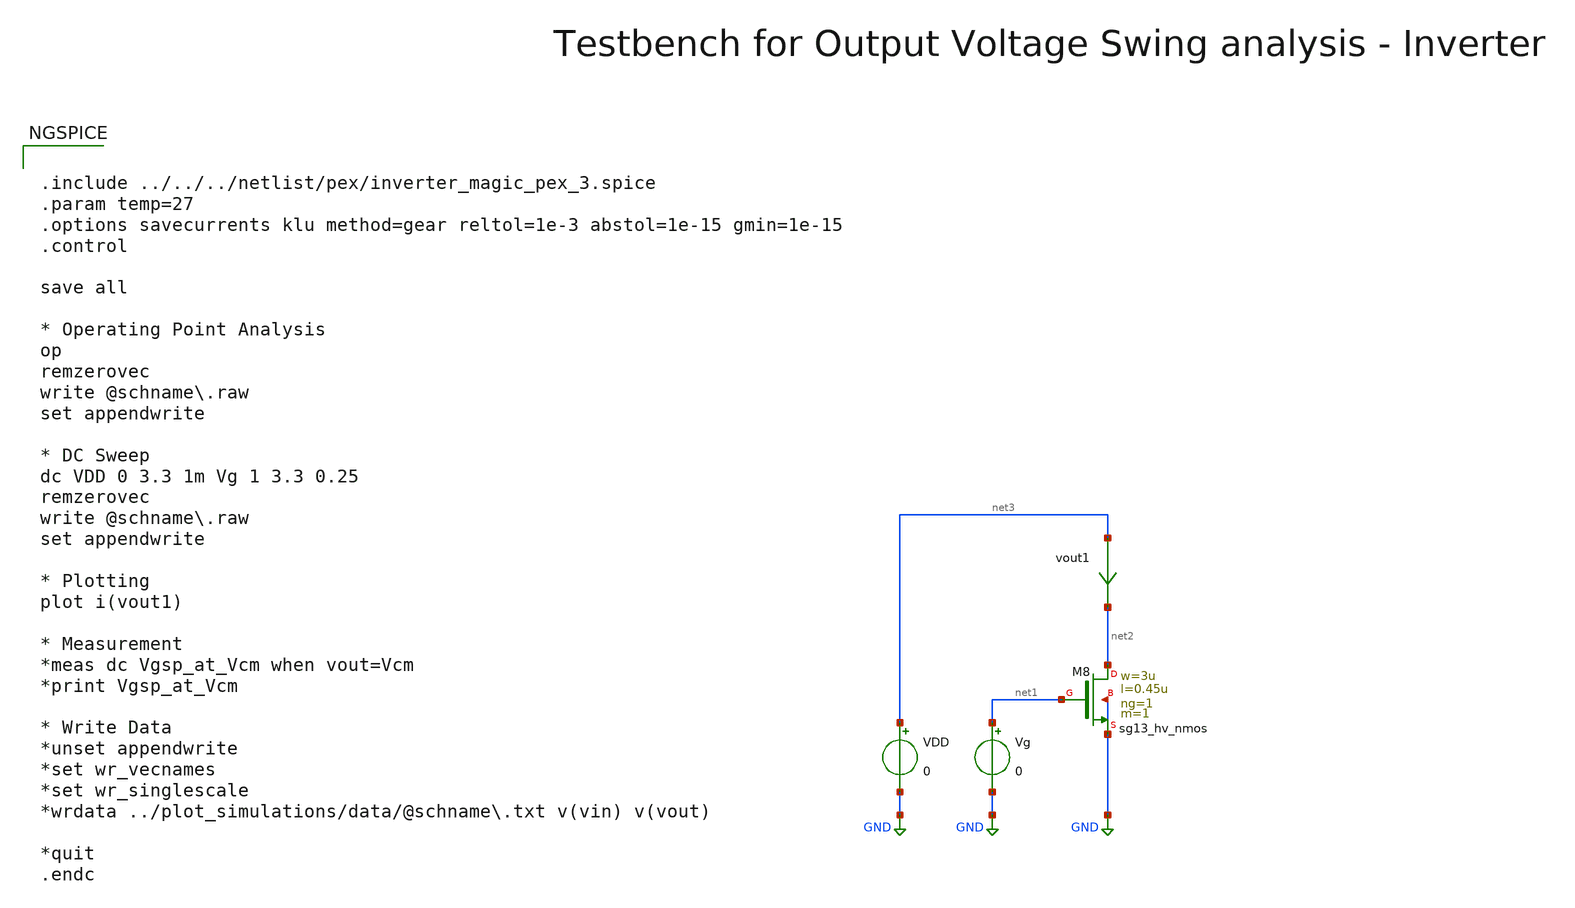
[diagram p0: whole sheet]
** sch_path: macros/heichips26_vcr/macros/switched_capacitor/testbenches/xschem/tb_nmos_dc.sch
**.subckt tb_nmos_dc
VDD net3 GND 0
Vg net1 GND 0
vout1 net3 net2 0
.save i(vout1)
XM8 net2 net1 GND GND sg13_hv_nmos w=3u l=0.45u ng=1 m=1 mm_ok=1
**** begin user architecture code


.include ../../../netlist/pex/inverter_magic_pex_3.spice
.param temp=27
.options savecurrents klu method=gear reltol=1e-3 abstol=1e-15 gmin=1e-15
.control

save all

* Operating Point Analysis
op
remzerovec
write @schname\.raw
set appendwrite

* DC Sweep
dc VDD 0 3.3 1m Vg 1 3.3 0.25
remzerovec
write @schname\.raw
set appendwrite

* Plotting
plot i(vout1)

* Measurement
*meas dc Vgsp_at_Vcm when vout=Vcm
*print Vgsp_at_Vcm

* Write Data
*unset appendwrite
*set wr_vecnames
*set wr_singlescale
*wrdata ../plot_simulations/data/@schname\.txt v(vin) v(vout)

*quit
.endc



.lib cornerMOSlv.lib mos_tt
.lib cornerMOShv.lib mos_tt
.lib cornerRES.lib res_typ
.lib cornerDIO.lib dio_tt

**** end user architecture code
**.ends
.GLOBAL GND
.end
